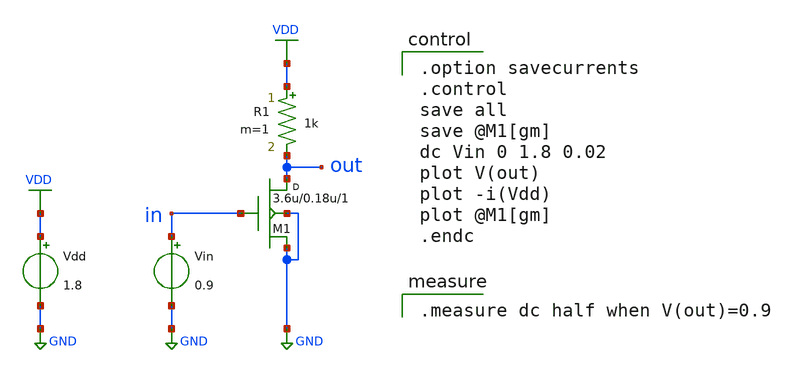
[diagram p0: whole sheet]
** sch_path: xschem/tb/dc_01.sch
**.subckt dc_01
Vdd VDD GND 1.8
Vin in GND 0.9
R1 VDD out 1k m=1
M1 out in GND GND nch w=3.6u l=0.18u m=1
**** begin user architecture code

.model nch nmos ( version=4.7 level=54 lmin=0.1u lmax=20u wmin=0.1u wmax=10u  )
.model pch pmos ( version=4.7 level=54 lmin=0.1u lmax=20u wmin=0.1u wmax=10u  )


.option savecurrents
.control
save all
save @M1[gm]
dc Vin 0 1.8 0.02
plot V(out)
plot -i(Vdd)
plot @M1[gm]
.endc


.measure dc half when V(out)=0.9

**** end user architecture code
**.ends
.GLOBAL VDD
.GLOBAL GND
.end
